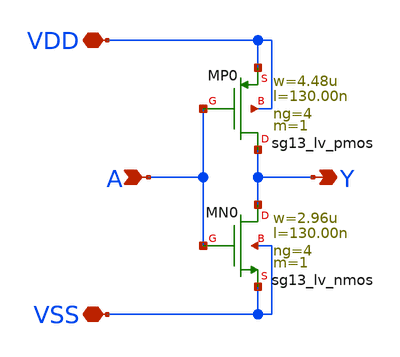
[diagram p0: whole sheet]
** sch_path: xschem/inv_4.sch
**.subckt inv_4 Y A VDD VSS
*.opin Y
*.ipin A
*.iopin VDD
*.iopin VSS
XMN0 Y A VSS VSS sg13_lv_nmos w=2.96u l=130.00n ng=4 m=1 mm_ok=1
XMP0 Y A VDD VDD sg13_lv_pmos w=4.48u l=130.00n ng=4 m=1 mm_ok=1
**.ends
.end
